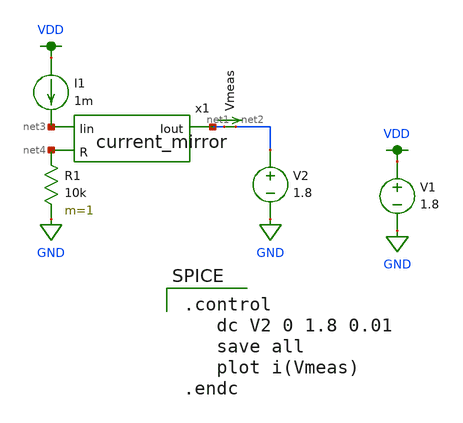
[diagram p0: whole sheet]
** sch_path: modules/current_mirror_test.sch
**.subckt current_mirror_test
x1 net1 net3 net4 current_mirror
I1 VDD net3 1m
V1 VDD GND 1.8
Vmeas net1 net2 0
.save i(vmeas)
V2 net2 GND 1.8
R1 net4 GND 10k m=1
**** begin user architecture code

.option wnflag=1
.param MC_SWITCH=0.0
.lib ~/skywater/skywater-pdk/libraries/sky130_fd_pr_ngspice/latest/models/sky130.lib.spice tt


.control
   dc V2 0 1.8 0.01
   save all
   plot i(Vmeas)
.endc

**** end user architecture code
**.ends

* expanding   symbol:  /home/madvlsi/R2R-DAC/current_mirror.sym # of pins=3
** sym_path: modules/current_mirror.sym
** sch_path: modules/current_mirror.sch
.subckt current_mirror Iout Iin R
*.ipin R
*.opin Iout
*.ipin Iin
XM2 R Iin Iin GND sky130_fd_pr__nfet_01v8 L=0.5 W=96 nf=1 ad='int((nf+1)/2) * W/nf * 0.29' as='int((nf+2)/2) * W/nf * 0.29'
+ pd='2*int((nf+1)/2) * (W/nf + 0.29)' ps='2*int((nf+2)/2) * (W/nf + 0.29)' nrd='0.29 / W' nrs='0.29 / W'
+ sa=0 sb=0 sd=0 mult=1 m=1
XM3 VDD net1 net1 VDD sky130_fd_pr__pfet_01v8 L=0.5 W=12 nf=1 ad='int((nf+1)/2) * W/nf * 0.29' as='int((nf+2)/2) * W/nf * 0.29'
+ pd='2*int((nf+1)/2) * (W/nf + 0.29)' ps='2*int((nf+2)/2) * (W/nf + 0.29)' nrd='0.29 / W' nrs='0.29 / W'
+ sa=0 sb=0 sd=0 mult=1 m=1
XM4 net2 net1 VDD VDD sky130_fd_pr__pfet_01v8 L=0.5 W=12 nf=1 ad='int((nf+1)/2) * W/nf * 0.29' as='int((nf+2)/2) * W/nf * 0.29'
+ pd='2*int((nf+1)/2) * (W/nf + 0.29)' ps='2*int((nf+2)/2) * (W/nf + 0.29)' nrd='0.29 / W' nrs='0.29 / W'
+ sa=0 sb=0 sd=0 mult=1 m=1
XM5 net3 net2 VDD VDD sky130_fd_pr__pfet_01v8 L=0.5 W=12 nf=1 ad='int((nf+1)/2) * W/nf * 0.29' as='int((nf+2)/2) * W/nf * 0.29'
+ pd='2*int((nf+1)/2) * (W/nf + 0.29)' ps='2*int((nf+2)/2) * (W/nf + 0.29)' nrd='0.29 / W' nrs='0.29 / W'
+ sa=0 sb=0 sd=0 mult=1 m=1
XM7 Iout net2 VDD VDD sky130_fd_pr__pfet_01v8 L=0.5 W=12 nf=1 ad='int((nf+1)/2) * W/nf * 0.29' as='int((nf+2)/2) * W/nf * 0.29'
+ pd='2*int((nf+1)/2) * (W/nf + 0.29)' ps='2*int((nf+2)/2) * (W/nf + 0.29)' nrd='0.29 / W' nrs='0.29 / W'
+ sa=0 sb=0 sd=0 mult=1 m=1
XM6 net1 Iin GND GND sky130_fd_pr__nfet_01v8 L=0.5 W=12 nf=1 ad='int((nf+1)/2) * W/nf * 0.29' as='int((nf+2)/2) * W/nf * 0.29'
+ pd='2*int((nf+1)/2) * (W/nf + 0.29)' ps='2*int((nf+2)/2) * (W/nf + 0.29)' nrd='0.29 / W' nrs='0.29 / W'
+ sa=0 sb=0 sd=0 mult=1 m=1
XM8 GND net3 net2 GND sky130_fd_pr__nfet_01v8 L=0.5 W=12 nf=1 ad='int((nf+1)/2) * W/nf * 0.29' as='int((nf+2)/2) * W/nf * 0.29'
+ pd='2*int((nf+1)/2) * (W/nf + 0.29)' ps='2*int((nf+2)/2) * (W/nf + 0.29)' nrd='0.29 / W' nrs='0.29 / W'
+ sa=0 sb=0 sd=0 mult=1 m=1
XM9 net3 net3 GND GND sky130_fd_pr__nfet_01v8 L=0.5 W=12 nf=1 ad='int((nf+1)/2) * W/nf * 0.29' as='int((nf+2)/2) * W/nf * 0.29'
+ pd='2*int((nf+1)/2) * (W/nf + 0.29)' ps='2*int((nf+2)/2) * (W/nf + 0.29)' nrd='0.29 / W' nrs='0.29 / W'
+ sa=0 sb=0 sd=0 mult=1 m=1
.ends

.GLOBAL GND
.GLOBAL VDD
.end
